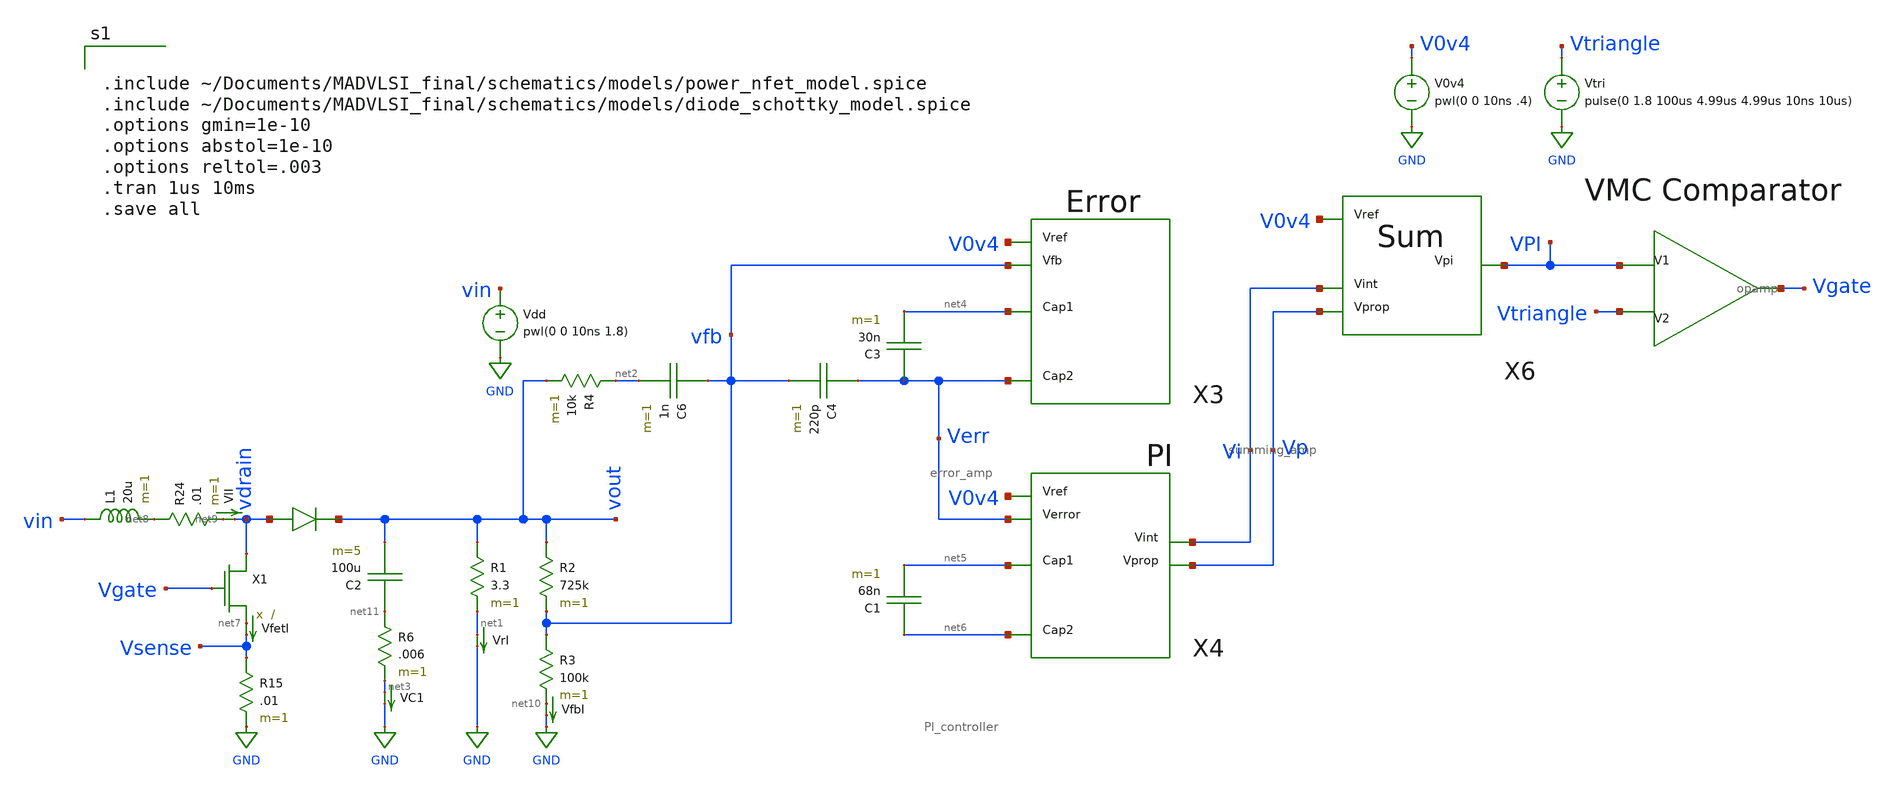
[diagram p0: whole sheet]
** sch_path: schematics/boost_controller_VMC.sch
**.subckt boost_controller_VMC
VfetI net7 Vsense 0
.save i(vfeti)
X1 vdrain Vgate net7 power_nfet
L1 vin net8 20u m=1
D1 vdrain vout diode_schottky
R1 vout net1 3.3 m=1
VlI net9 vdrain 0
.save i(vli)
VrI net1 GND 0
.save i(vri)
R2 vout vfb 725k m=1
R3 vfb net10 100k m=1
V0v4 V0v4 GND pwl(0 0 10ns .4)
R24 net8 net9 .01 m=1
VfbI net10 GND 0
.save i(vfbi)
C3 Verr net4 30n m=1
C4 Verr vfb 220p m=1
R4 net2 vout 10k m=1
C6 vfb net2 1n m=1
C2 net11 vout 100u m=5
R6 net11 net3 .006 m=1
VC1 net3 GND 0
.save i(vc1)
R15 Vsense GND .01 m=1
X3 V0v4 net4 vfb Verr error_amp
X4 V0v4 net5 Verr net6 Vi Vp PI_controller
C1 net6 net5 68n m=1
X6 V0v4 VPI Vi Vp summing_amp
X15 VPI Vtriangle Vgate opamp
Vtri Vtriangle GND pulse(0 1.8 100us 4.99us 4.99us 10ns 10us)
Vdd vin GND pwl(0 0 10ns 1.8)
**** begin user architecture code


.include ~/Documents/MADVLSI_final/schematics/models/power_nfet_model.spice
.include ~/Documents/MADVLSI_final/schematics/models/diode_schottky_model.spice
.options gmin=1e-10
.options abstol=1e-10
.options reltol=.003
.tran 1us 10ms
.save all


.option wnflag=1
.lib ~/skywater/skywater-pdk/libraries/sky130_fd_pr_ngspice/latest/models/sky130.lib.spice tt

**** end user architecture code
**.ends

* expanding   symbol:  /home/madvlsi/Documents/MADVLSI_final/schematics/error_amp.sym # of pins=4
** sym_path: schematics/error_amp.sym
** sch_path: schematics/error_amp.sch
.subckt error_amp Vref Cap1 Vfb Cap2
*.ipin Vfb
*.ipin Vref
*.iopin Cap1
*.iopin Cap2
XR1 Cap1 Vfb GND sky130_fd_pr__res_xhigh_po_0p35 L=8.65 mult=1 m=1
X1 Vref Vfb Cap2 opamp
.ends


* expanding   symbol:  /home/madvlsi/Documents/MADVLSI_final/schematics/PI_controller.sym # of
*+ pins=6
** sym_path: schematics/PI_controller.sym
** sch_path: schematics/PI_controller.sch
.subckt PI_controller Vref Cap1 Verror Cap2 Vint Vprop
*.ipin Verror
*.ipin Vref
*.iopin Cap1
*.iopin Cap2
*.opin Vint
*.opin Vprop
XR1 net1 net2 GND sky130_fd_pr__res_xhigh_po_0p35 L=1.65 mult=1 m=1
XR2 Vref net1 GND sky130_fd_pr__res_xhigh_po_0p35 L=1.65 mult=1 m=1
XR3 Verror Cap1 GND sky130_fd_pr__res_xhigh_po_0p35 L=1.65 mult=1 m=1
XR4 Cap1 Cap2 GND sky130_fd_pr__res_xhigh_po_0p35 L=8.65 mult=1 m=1
XR5 Cap2 net3 GND sky130_fd_pr__res_xhigh_po_0p35 L=1.65 mult=1 m=1
XR6 net3 Vint GND sky130_fd_pr__res_xhigh_po_0p35 L=8.65 mult=1 m=1
X1 Vref Cap1 Cap2 opamp
X2 Vref net3 Vint opamp
X3 net1 Vprop Vprop opamp
X4 Verror net2 net2 opamp
.ends


* expanding   symbol:  /home/madvlsi/Documents/MADVLSI_final/schematics/summing_amp.sym # of pins=4
** sym_path: schematics/summing_amp.sym
** sch_path: schematics/summing_amp.sch
.subckt summing_amp Vref Vpi Vint Vprop
*.ipin Vref
*.ipin Vint
*.ipin Vprop
*.opin Vpi
XR3 net1 Vint GND sky130_fd_pr__res_xhigh_po_0p35 L=1.65 mult=1 m=1
XR5 Vprop net1 GND sky130_fd_pr__res_xhigh_po_0p35 L=1.65 mult=1 m=1
XR1 net2 Vpi GND sky130_fd_pr__res_xhigh_po_0p35 L=1.65 mult=1 m=1
XR2 Vref net2 GND sky130_fd_pr__res_xhigh_po_0p35 L=1.65 mult=1 m=1
X1 net1 net2 Vpi opamp
.ends


* expanding   symbol:  /home/madvlsi/Documents/MADVLSI_final/schematics/opamp.sym # of pins=3
** sym_path: schematics/opamp.sym
** sch_path: schematics/opamp.sch
.subckt opamp V1 V2 VOUT
*.ipin V1
*.ipin V2
*.opin VOUT
XM19 net12 net10 GND VDD sky130_fd_pr__pfet_01v8 L=.6 W=1.5 nf=1 ad='int((nf+1)/2) * W/nf * 0.29' as='int((nf+2)/2) * W/nf * 0.29'
+ pd='2*int((nf+1)/2) * (W/nf + 0.29)' ps='2*int((nf+2)/2) * (W/nf + 0.29)' nrd='0.29 / W' nrs='0.29 / W'
+ sa=0 sb=0 sd=0 mult=1 m=1
XMD20 VDD VDD net12 VDD sky130_fd_pr__pfet_01v8 L=.6 W=1.5 nf=1 ad='int((nf+1)/2) * W/nf * 0.29' as='int((nf+2)/2) * W/nf * 0.29'
+ pd='2*int((nf+1)/2) * (W/nf + 0.29)' ps='2*int((nf+2)/2) * (W/nf + 0.29)' nrd='0.29 / W' nrs='0.29 / W'
+ sa=0 sb=0 sd=0 mult=1 m=1
XM22 net12 net10 net9 VDD sky130_fd_pr__pfet_01v8 L=.6 W=1.5 nf=1 ad='int((nf+1)/2) * W/nf * 0.29' as='int((nf+2)/2) * W/nf * 0.29'
+ pd='2*int((nf+1)/2) * (W/nf + 0.29)' ps='2*int((nf+2)/2) * (W/nf + 0.29)' nrd='0.29 / W' nrs='0.29 / W'
+ sa=0 sb=0 sd=0 mult=1 m=1
XM23 GND net10 net12 VDD sky130_fd_pr__pfet_01v8 L=.6 W=1.5 nf=1 ad='int((nf+1)/2) * W/nf * 0.29' as='int((nf+2)/2) * W/nf * 0.29'
+ pd='2*int((nf+1)/2) * (W/nf + 0.29)' ps='2*int((nf+2)/2) * (W/nf + 0.29)' nrd='0.29 / W' nrs='0.29 / W'
+ sa=0 sb=0 sd=0 mult=1 m=1
XMD24 net9 VDD net10 VDD sky130_fd_pr__pfet_01v8 L=.6 W=1.5 nf=1 ad='int((nf+1)/2) * W/nf * 0.29' as='int((nf+2)/2) * W/nf * 0.29'
+ pd='2*int((nf+1)/2) * (W/nf + 0.29)' ps='2*int((nf+2)/2) * (W/nf + 0.29)' nrd='0.29 / W' nrs='0.29 / W'
+ sa=0 sb=0 sd=0 mult=1 m=1
XM25 VDD net10 net12 VDD sky130_fd_pr__pfet_01v8 L=.6 W=1.5 nf=1 ad='int((nf+1)/2) * W/nf * 0.29' as='int((nf+2)/2) * W/nf * 0.29'
+ pd='2*int((nf+1)/2) * (W/nf + 0.29)' ps='2*int((nf+2)/2) * (W/nf + 0.29)' nrd='0.29 / W' nrs='0.29 / W'
+ sa=0 sb=0 sd=0 mult=1 m=1
XM26 net7 V2 net11 VDD sky130_fd_pr__pfet_01v8 L=.6 W=1.5 nf=1 ad='int((nf+1)/2) * W/nf * 0.29' as='int((nf+2)/2) * W/nf * 0.29'
+ pd='2*int((nf+1)/2) * (W/nf + 0.29)' ps='2*int((nf+2)/2) * (W/nf + 0.29)' nrd='0.29 / W' nrs='0.29 / W'
+ sa=0 sb=0 sd=0 mult=1 m=1
XMD27 net5 VDD net14 VDD sky130_fd_pr__pfet_01v8 L=.6 W=1.5 nf=1 ad='int((nf+1)/2) * W/nf * 0.29' as='int((nf+2)/2) * W/nf * 0.29'
+ pd='2*int((nf+1)/2) * (W/nf + 0.29)' ps='2*int((nf+2)/2) * (W/nf + 0.29)' nrd='0.29 / W' nrs='0.29 / W'
+ sa=0 sb=0 sd=0 mult=1 m=1
XM28 net6 V1 net11 VDD sky130_fd_pr__pfet_01v8 L=.6 W=1.5 nf=1 ad='int((nf+1)/2) * W/nf * 0.29' as='int((nf+2)/2) * W/nf * 0.29'
+ pd='2*int((nf+1)/2) * (W/nf + 0.29)' ps='2*int((nf+2)/2) * (W/nf + 0.29)' nrd='0.29 / W' nrs='0.29 / W'
+ sa=0 sb=0 sd=0 mult=1 m=1
XM29 net11 net10 VDD VDD sky130_fd_pr__pfet_01v8 L=.6 W=1.5 nf=1 ad='int((nf+1)/2) * W/nf * 0.29' as='int((nf+2)/2) * W/nf * 0.29'
+ pd='2*int((nf+1)/2) * (W/nf + 0.29)' ps='2*int((nf+2)/2) * (W/nf + 0.29)' nrd='0.29 / W' nrs='0.29 / W'
+ sa=0 sb=0 sd=0 mult=1 m=1
XMD30 net11 VDD VDD VDD sky130_fd_pr__pfet_01v8 L=.6 W=1.5 nf=1 ad='int((nf+1)/2) * W/nf * 0.29' as='int((nf+2)/2) * W/nf * 0.29'
+ pd='2*int((nf+1)/2) * (W/nf + 0.29)' ps='2*int((nf+2)/2) * (W/nf + 0.29)' nrd='0.29 / W' nrs='0.29 / W'
+ sa=0 sb=0 sd=0 mult=1 m=1
XMD31 net2 VDD net13 VDD sky130_fd_pr__pfet_01v8 L=.6 W=1.5 nf=1 ad='int((nf+1)/2) * W/nf * 0.29' as='int((nf+2)/2) * W/nf * 0.29'
+ pd='2*int((nf+1)/2) * (W/nf + 0.29)' ps='2*int((nf+2)/2) * (W/nf + 0.29)' nrd='0.29 / W' nrs='0.29 / W'
+ sa=0 sb=0 sd=0 mult=1 m=1
XM32 net4 net5 net5 VDD sky130_fd_pr__pfet_01v8 L=.6 W=1.5 nf=1 ad='int((nf+1)/2) * W/nf * 0.29' as='int((nf+2)/2) * W/nf * 0.29'
+ pd='2*int((nf+1)/2) * (W/nf + 0.29)' ps='2*int((nf+2)/2) * (W/nf + 0.29)' nrd='0.29 / W' nrs='0.29 / W'
+ sa=0 sb=0 sd=0 mult=1 m=1
XM33 VDD net10 net4 VDD sky130_fd_pr__pfet_01v8 L=.6 W=1.5 nf=1 ad='int((nf+1)/2) * W/nf * 0.29' as='int((nf+2)/2) * W/nf * 0.29'
+ pd='2*int((nf+1)/2) * (W/nf + 0.29)' ps='2*int((nf+2)/2) * (W/nf + 0.29)' nrd='0.29 / W' nrs='0.29 / W'
+ sa=0 sb=0 sd=0 mult=1 m=1
XM34 net3 net5 net2 VDD sky130_fd_pr__pfet_01v8 L=.6 W=1.5 nf=1 ad='int((nf+1)/2) * W/nf * 0.29' as='int((nf+2)/2) * W/nf * 0.29'
+ pd='2*int((nf+1)/2) * (W/nf + 0.29)' ps='2*int((nf+2)/2) * (W/nf + 0.29)' nrd='0.29 / W' nrs='0.29 / W'
+ sa=0 sb=0 sd=0 mult=1 m=1
XM35 VDD net10 net3 VDD sky130_fd_pr__pfet_01v8 L=.6 W=1.5 nf=1 ad='int((nf+1)/2) * W/nf * 0.29' as='int((nf+2)/2) * W/nf * 0.29'
+ pd='2*int((nf+1)/2) * (W/nf + 0.29)' ps='2*int((nf+2)/2) * (W/nf + 0.29)' nrd='0.29 / W' nrs='0.29 / W'
+ sa=0 sb=0 sd=0 mult=1 m=1
XM36 VOUT net2 VDD VDD sky130_fd_pr__pfet_01v8 L=.6 W=1.5 nf=1 ad='int((nf+1)/2) * W/nf * 0.29' as='int((nf+2)/2) * W/nf * 0.29'
+ pd='2*int((nf+1)/2) * (W/nf + 0.29)' ps='2*int((nf+2)/2) * (W/nf + 0.29)' nrd='0.29 / W' nrs='0.29 / W'
+ sa=0 sb=0 sd=0 mult=1 m=1
XM37 VDD net2 VOUT VDD sky130_fd_pr__pfet_01v8 L=.6 W=1.5 nf=1 ad='int((nf+1)/2) * W/nf * 0.29' as='int((nf+2)/2) * W/nf * 0.29'
+ pd='2*int((nf+1)/2) * (W/nf + 0.29)' ps='2*int((nf+2)/2) * (W/nf + 0.29)' nrd='0.29 / W' nrs='0.29 / W'
+ sa=0 sb=0 sd=0 mult=1 m=1
XM38 VOUT net2 VDD VDD sky130_fd_pr__pfet_01v8 L=.6 W=1.5 nf=1 ad='int((nf+1)/2) * W/nf * 0.29' as='int((nf+2)/2) * W/nf * 0.29'
+ pd='2*int((nf+1)/2) * (W/nf + 0.29)' ps='2*int((nf+2)/2) * (W/nf + 0.29)' nrd='0.29 / W' nrs='0.29 / W'
+ sa=0 sb=0 sd=0 mult=1 m=1
XM39 VDD net2 VOUT VDD sky130_fd_pr__pfet_01v8 L=.6 W=1.5 nf=1 ad='int((nf+1)/2) * W/nf * 0.29' as='int((nf+2)/2) * W/nf * 0.29'
+ pd='2*int((nf+1)/2) * (W/nf + 0.29)' ps='2*int((nf+2)/2) * (W/nf + 0.29)' nrd='0.29 / W' nrs='0.29 / W'
+ sa=0 sb=0 sd=0 mult=1 m=1
XM40 net1 net9 VDD GND sky130_fd_pr__nfet_01v8 L=.6 W=1.5 nf=1 ad='int((nf+1)/2) * W/nf * 0.29' as='int((nf+2)/2) * W/nf * 0.29'
+ pd='2*int((nf+1)/2) * (W/nf + 0.29)' ps='2*int((nf+2)/2) * (W/nf + 0.29)' nrd='0.29 / W' nrs='0.29 / W'
+ sa=0 sb=0 sd=0 mult=1 m=1
XMD41 GND GND net1 GND sky130_fd_pr__nfet_01v8 L=.6 W=1.5 nf=1 ad='int((nf+1)/2) * W/nf * 0.29' as='int((nf+2)/2) * W/nf * 0.29'
+ pd='2*int((nf+1)/2) * (W/nf + 0.29)' ps='2*int((nf+2)/2) * (W/nf + 0.29)' nrd='0.29 / W' nrs='0.29 / W'
+ sa=0 sb=0 sd=0 mult=1 m=1
XM42 net1 net9 net10 GND sky130_fd_pr__nfet_01v8 L=.6 W=1.5 nf=1 ad='int((nf+1)/2) * W/nf * 0.29' as='int((nf+2)/2) * W/nf * 0.29'
+ pd='2*int((nf+1)/2) * (W/nf + 0.29)' ps='2*int((nf+2)/2) * (W/nf + 0.29)' nrd='0.29 / W' nrs='0.29 / W'
+ sa=0 sb=0 sd=0 mult=1 m=1
XM43 VDD net9 net1 GND sky130_fd_pr__nfet_01v8 L=.6 W=1.5 nf=1 ad='int((nf+1)/2) * W/nf * 0.29' as='int((nf+2)/2) * W/nf * 0.29'
+ pd='2*int((nf+1)/2) * (W/nf + 0.29)' ps='2*int((nf+2)/2) * (W/nf + 0.29)' nrd='0.29 / W' nrs='0.29 / W'
+ sa=0 sb=0 sd=0 mult=1 m=1
XMD44 net10 GND net9 GND sky130_fd_pr__nfet_01v8 L=.6 W=1.5 nf=1 ad='int((nf+1)/2) * W/nf * 0.29' as='int((nf+2)/2) * W/nf * 0.29'
+ pd='2*int((nf+1)/2) * (W/nf + 0.29)' ps='2*int((nf+2)/2) * (W/nf + 0.29)' nrd='0.29 / W' nrs='0.29 / W'
+ sa=0 sb=0 sd=0 mult=1 m=1
XM45 GND net9 net1 GND sky130_fd_pr__nfet_01v8 L=.6 W=1.5 nf=1 ad='int((nf+1)/2) * W/nf * 0.29' as='int((nf+2)/2) * W/nf * 0.29'
+ pd='2*int((nf+1)/2) * (W/nf + 0.29)' ps='2*int((nf+2)/2) * (W/nf + 0.29)' nrd='0.29 / W' nrs='0.29 / W'
+ sa=0 sb=0 sd=0 mult=1 m=1
XM46 net3 V1 net8 GND sky130_fd_pr__nfet_01v8 L=.6 W=1.5 nf=1 ad='int((nf+1)/2) * W/nf * 0.29' as='int((nf+2)/2) * W/nf * 0.29'
+ pd='2*int((nf+1)/2) * (W/nf + 0.29)' ps='2*int((nf+2)/2) * (W/nf + 0.29)' nrd='0.29 / W' nrs='0.29 / W'
+ sa=0 sb=0 sd=0 mult=1 m=1
XMD47 net5 GND net15 GND sky130_fd_pr__nfet_01v8 L=.6 W=1.5 nf=1 ad='int((nf+1)/2) * W/nf * 0.29' as='int((nf+2)/2) * W/nf * 0.29'
+ pd='2*int((nf+1)/2) * (W/nf + 0.29)' ps='2*int((nf+2)/2) * (W/nf + 0.29)' nrd='0.29 / W' nrs='0.29 / W'
+ sa=0 sb=0 sd=0 mult=1 m=1
XM48 net4 V2 net8 GND sky130_fd_pr__nfet_01v8 L=.6 W=1.5 nf=1 ad='int((nf+1)/2) * W/nf * 0.29' as='int((nf+2)/2) * W/nf * 0.29'
+ pd='2*int((nf+1)/2) * (W/nf + 0.29)' ps='2*int((nf+2)/2) * (W/nf + 0.29)' nrd='0.29 / W' nrs='0.29 / W'
+ sa=0 sb=0 sd=0 mult=1 m=1
XM49 net8 net9 GND GND sky130_fd_pr__nfet_01v8 L=.6 W=1.5 nf=1 ad='int((nf+1)/2) * W/nf * 0.29' as='int((nf+2)/2) * W/nf * 0.29'
+ pd='2*int((nf+1)/2) * (W/nf + 0.29)' ps='2*int((nf+2)/2) * (W/nf + 0.29)' nrd='0.29 / W' nrs='0.29 / W'
+ sa=0 sb=0 sd=0 mult=1 m=1
XMD50 net8 GND GND GND sky130_fd_pr__nfet_01v8 L=.6 W=1.5 nf=1 ad='int((nf+1)/2) * W/nf * 0.29' as='int((nf+2)/2) * W/nf * 0.29'
+ pd='2*int((nf+1)/2) * (W/nf + 0.29)' ps='2*int((nf+2)/2) * (W/nf + 0.29)' nrd='0.29 / W' nrs='0.29 / W'
+ sa=0 sb=0 sd=0 mult=1 m=1
XMD51 net2 GND net16 GND sky130_fd_pr__nfet_01v8 L=.6 W=1.5 nf=1 ad='int((nf+1)/2) * W/nf * 0.29' as='int((nf+2)/2) * W/nf * 0.29'
+ pd='2*int((nf+1)/2) * (W/nf + 0.29)' ps='2*int((nf+2)/2) * (W/nf + 0.29)' nrd='0.29 / W' nrs='0.29 / W'
+ sa=0 sb=0 sd=0 mult=1 m=1
XM52 GND net9 net7 GND sky130_fd_pr__nfet_01v8 L=.6 W=1.5 nf=1 ad='int((nf+1)/2) * W/nf * 0.29' as='int((nf+2)/2) * W/nf * 0.29'
+ pd='2*int((nf+1)/2) * (W/nf + 0.29)' ps='2*int((nf+2)/2) * (W/nf + 0.29)' nrd='0.29 / W' nrs='0.29 / W'
+ sa=0 sb=0 sd=0 mult=1 m=1
XMD53 VOUT GND GND GND sky130_fd_pr__nfet_01v8 L=.6 W=1.5 nf=1 ad='int((nf+1)/2) * W/nf * 0.29' as='int((nf+2)/2) * W/nf * 0.29'
+ pd='2*int((nf+1)/2) * (W/nf + 0.29)' ps='2*int((nf+2)/2) * (W/nf + 0.29)' nrd='0.29 / W' nrs='0.29 / W'
+ sa=0 sb=0 sd=0 mult=1 m=1
XM54 GND net9 net6 GND sky130_fd_pr__nfet_01v8 L=.6 W=1.5 nf=1 ad='int((nf+1)/2) * W/nf * 0.29' as='int((nf+2)/2) * W/nf * 0.29'
+ pd='2*int((nf+1)/2) * (W/nf + 0.29)' ps='2*int((nf+2)/2) * (W/nf + 0.29)' nrd='0.29 / W' nrs='0.29 / W'
+ sa=0 sb=0 sd=0 mult=1 m=1
XM55 net7 net5 net5 GND sky130_fd_pr__nfet_01v8 L=.6 W=1.5 nf=1 ad='int((nf+1)/2) * W/nf * 0.29' as='int((nf+2)/2) * W/nf * 0.29'
+ pd='2*int((nf+1)/2) * (W/nf + 0.29)' ps='2*int((nf+2)/2) * (W/nf + 0.29)' nrd='0.29 / W' nrs='0.29 / W'
+ sa=0 sb=0 sd=0 mult=1 m=1
XM56 net6 net5 net2 GND sky130_fd_pr__nfet_01v8 L=.6 W=1.5 nf=1 ad='int((nf+1)/2) * W/nf * 0.29' as='int((nf+2)/2) * W/nf * 0.29'
+ pd='2*int((nf+1)/2) * (W/nf + 0.29)' ps='2*int((nf+2)/2) * (W/nf + 0.29)' nrd='0.29 / W' nrs='0.29 / W'
+ sa=0 sb=0 sd=0 mult=1 m=1
XMD57 VOUT GND GND GND sky130_fd_pr__nfet_01v8 L=.6 W=1.5 nf=1 ad='int((nf+1)/2) * W/nf * 0.29' as='int((nf+2)/2) * W/nf * 0.29'
+ pd='2*int((nf+1)/2) * (W/nf + 0.29)' ps='2*int((nf+2)/2) * (W/nf + 0.29)' nrd='0.29 / W' nrs='0.29 / W'
+ sa=0 sb=0 sd=0 mult=1 m=1
XM58 GND net2 VOUT GND sky130_fd_pr__nfet_01v8 L=.6 W=1.5 nf=1 ad='int((nf+1)/2) * W/nf * 0.29' as='int((nf+2)/2) * W/nf * 0.29'
+ pd='2*int((nf+1)/2) * (W/nf + 0.29)' ps='2*int((nf+2)/2) * (W/nf + 0.29)' nrd='0.29 / W' nrs='0.29 / W'
+ sa=0 sb=0 sd=0 mult=1 m=1
XM59 GND net2 VOUT GND sky130_fd_pr__nfet_01v8 L=.6 W=1.5 nf=1 ad='int((nf+1)/2) * W/nf * 0.29' as='int((nf+2)/2) * W/nf * 0.29'
+ pd='2*int((nf+1)/2) * (W/nf + 0.29)' ps='2*int((nf+2)/2) * (W/nf + 0.29)' nrd='0.29 / W' nrs='0.29 / W'
+ sa=0 sb=0 sd=0 mult=1 m=1
XM60 net12 net10 GND VDD sky130_fd_pr__pfet_01v8 L=.6 W=1.5 nf=1 ad='int((nf+1)/2) * W/nf * 0.29' as='int((nf+2)/2) * W/nf * 0.29'
+ pd='2*int((nf+1)/2) * (W/nf + 0.29)' ps='2*int((nf+2)/2) * (W/nf + 0.29)' nrd='0.29 / W' nrs='0.29 / W'
+ sa=0 sb=0 sd=0 mult=1 m=1
XM61 net10 net10 net4 VDD sky130_fd_pr__pfet_01v8 L=.6 W=1.5 nf=1 ad='int((nf+1)/2) * W/nf * 0.29' as='int((nf+2)/2) * W/nf * 0.29'
+ pd='2*int((nf+1)/2) * (W/nf + 0.29)' ps='2*int((nf+2)/2) * (W/nf + 0.29)' nrd='0.29 / W' nrs='0.29 / W'
+ sa=0 sb=0 sd=0 mult=1 m=1
XM62 net1 net9 VDD GND sky130_fd_pr__nfet_01v8 L=.6 W=1.5 nf=1 ad='int((nf+1)/2) * W/nf * 0.29' as='int((nf+2)/2) * W/nf * 0.29'
+ pd='2*int((nf+1)/2) * (W/nf + 0.29)' ps='2*int((nf+2)/2) * (W/nf + 0.29)' nrd='0.29 / W' nrs='0.29 / W'
+ sa=0 sb=0 sd=0 mult=1 m=1
XM63 net9 net9 net7 GND sky130_fd_pr__nfet_01v8 L=.6 W=1.5 nf=1 ad='int((nf+1)/2) * W/nf * 0.29' as='int((nf+2)/2) * W/nf * 0.29'
+ pd='2*int((nf+1)/2) * (W/nf + 0.29)' ps='2*int((nf+2)/2) * (W/nf + 0.29)' nrd='0.29 / W' nrs='0.29 / W'
+ sa=0 sb=0 sd=0 mult=1 m=1
XMD64 VDD GND GND GND sky130_fd_pr__nfet_01v8 L=.6 W=1.5 nf=1 ad='int((nf+1)/2) * W/nf * 0.29' as='int((nf+2)/2) * W/nf * 0.29'
+ pd='2*int((nf+1)/2) * (W/nf + 0.29)' ps='2*int((nf+2)/2) * (W/nf + 0.29)' nrd='0.29 / W' nrs='0.29 / W'
+ sa=0 sb=0 sd=0 mult=1 m=1
XMD65 net7 GND GND GND sky130_fd_pr__nfet_01v8 L=.6 W=1.5 nf=1 ad='int((nf+1)/2) * W/nf * 0.29' as='int((nf+2)/2) * W/nf * 0.29'
+ pd='2*int((nf+1)/2) * (W/nf + 0.29)' ps='2*int((nf+2)/2) * (W/nf + 0.29)' nrd='0.29 / W' nrs='0.29 / W'
+ sa=0 sb=0 sd=0 mult=1 m=1
XMD66 GND VDD VDD VDD sky130_fd_pr__pfet_01v8 L=.6 W=1.5 nf=1 ad='int((nf+1)/2) * W/nf * 0.29' as='int((nf+2)/2) * W/nf * 0.29'
+ pd='2*int((nf+1)/2) * (W/nf + 0.29)' ps='2*int((nf+2)/2) * (W/nf + 0.29)' nrd='0.29 / W' nrs='0.29 / W'
+ sa=0 sb=0 sd=0 mult=1 m=1
XMD67 net4 VDD VDD VDD sky130_fd_pr__pfet_01v8 L=.6 W=1.5 nf=1 ad='int((nf+1)/2) * W/nf * 0.29' as='int((nf+2)/2) * W/nf * 0.29'
+ pd='2*int((nf+1)/2) * (W/nf + 0.29)' ps='2*int((nf+2)/2) * (W/nf + 0.29)' nrd='0.29 / W' nrs='0.29 / W'
+ sa=0 sb=0 sd=0 mult=1 m=1
XMD1 net15 GND net3 GND sky130_fd_pr__nfet_01v8 L=.6 W=1.5 nf=1 ad='int((nf+1)/2) * W/nf * 0.29' as='int((nf+2)/2) * W/nf * 0.29'
+ pd='2*int((nf+1)/2) * (W/nf + 0.29)' ps='2*int((nf+2)/2) * (W/nf + 0.29)' nrd='0.29 / W' nrs='0.29 / W'
+ sa=0 sb=0 sd=0 mult=1 m=1
XMD2 net16 GND net4 GND sky130_fd_pr__nfet_01v8 L=.6 W=1.5 nf=1 ad='int((nf+1)/2) * W/nf * 0.29' as='int((nf+2)/2) * W/nf * 0.29'
+ pd='2*int((nf+1)/2) * (W/nf + 0.29)' ps='2*int((nf+2)/2) * (W/nf + 0.29)' nrd='0.29 / W' nrs='0.29 / W'
+ sa=0 sb=0 sd=0 mult=1 m=1
XMD3 net13 VDD net6 VDD sky130_fd_pr__pfet_01v8 L=.6 W=1.5 nf=1 ad='int((nf+1)/2) * W/nf * 0.29' as='int((nf+2)/2) * W/nf * 0.29'
+ pd='2*int((nf+1)/2) * (W/nf + 0.29)' ps='2*int((nf+2)/2) * (W/nf + 0.29)' nrd='0.29 / W' nrs='0.29 / W'
+ sa=0 sb=0 sd=0 mult=1 m=1
XMD4 net14 VDD net7 VDD sky130_fd_pr__pfet_01v8 L=.6 W=1.5 nf=1 ad='int((nf+1)/2) * W/nf * 0.29' as='int((nf+2)/2) * W/nf * 0.29'
+ pd='2*int((nf+1)/2) * (W/nf + 0.29)' ps='2*int((nf+2)/2) * (W/nf + 0.29)' nrd='0.29 / W' nrs='0.29 / W'
+ sa=0 sb=0 sd=0 mult=1 m=1
XM1 net21 net10 GND VDD sky130_fd_pr__pfet_01v8 L=.6 W=1.5 nf=1 ad='int((nf+1)/2) * W/nf * 0.29' as='int((nf+2)/2) * W/nf * 0.29'
+ pd='2*int((nf+1)/2) * (W/nf + 0.29)' ps='2*int((nf+2)/2) * (W/nf + 0.29)' nrd='0.29 / W' nrs='0.29 / W'
+ sa=0 sb=0 sd=0 mult=1 m=1
XMD5 VDD VDD net21 VDD sky130_fd_pr__pfet_01v8 L=.6 W=1.5 nf=1 ad='int((nf+1)/2) * W/nf * 0.29' as='int((nf+2)/2) * W/nf * 0.29'
+ pd='2*int((nf+1)/2) * (W/nf + 0.29)' ps='2*int((nf+2)/2) * (W/nf + 0.29)' nrd='0.29 / W' nrs='0.29 / W'
+ sa=0 sb=0 sd=0 mult=1 m=1
XM6 net21 net10 net9 VDD sky130_fd_pr__pfet_01v8 L=.6 W=1.5 nf=1 ad='int((nf+1)/2) * W/nf * 0.29' as='int((nf+2)/2) * W/nf * 0.29'
+ pd='2*int((nf+1)/2) * (W/nf + 0.29)' ps='2*int((nf+2)/2) * (W/nf + 0.29)' nrd='0.29 / W' nrs='0.29 / W'
+ sa=0 sb=0 sd=0 mult=1 m=1
XM7 GND net10 net21 VDD sky130_fd_pr__pfet_01v8 L=.6 W=1.5 nf=1 ad='int((nf+1)/2) * W/nf * 0.29' as='int((nf+2)/2) * W/nf * 0.29'
+ pd='2*int((nf+1)/2) * (W/nf + 0.29)' ps='2*int((nf+2)/2) * (W/nf + 0.29)' nrd='0.29 / W' nrs='0.29 / W'
+ sa=0 sb=0 sd=0 mult=1 m=1
XMD8 net9 VDD net10 VDD sky130_fd_pr__pfet_01v8 L=.6 W=1.5 nf=1 ad='int((nf+1)/2) * W/nf * 0.29' as='int((nf+2)/2) * W/nf * 0.29'
+ pd='2*int((nf+1)/2) * (W/nf + 0.29)' ps='2*int((nf+2)/2) * (W/nf + 0.29)' nrd='0.29 / W' nrs='0.29 / W'
+ sa=0 sb=0 sd=0 mult=1 m=1
XM9 VDD net10 net21 VDD sky130_fd_pr__pfet_01v8 L=.6 W=1.5 nf=1 ad='int((nf+1)/2) * W/nf * 0.29' as='int((nf+2)/2) * W/nf * 0.29'
+ pd='2*int((nf+1)/2) * (W/nf + 0.29)' ps='2*int((nf+2)/2) * (W/nf + 0.29)' nrd='0.29 / W' nrs='0.29 / W'
+ sa=0 sb=0 sd=0 mult=1 m=1
XM10 net7 V2 net20 VDD sky130_fd_pr__pfet_01v8 L=.6 W=1.5 nf=1 ad='int((nf+1)/2) * W/nf * 0.29' as='int((nf+2)/2) * W/nf * 0.29'
+ pd='2*int((nf+1)/2) * (W/nf + 0.29)' ps='2*int((nf+2)/2) * (W/nf + 0.29)' nrd='0.29 / W' nrs='0.29 / W'
+ sa=0 sb=0 sd=0 mult=1 m=1
XMD11 net18 VDD net23 VDD sky130_fd_pr__pfet_01v8 L=.6 W=1.5 nf=1 ad='int((nf+1)/2) * W/nf * 0.29' as='int((nf+2)/2) * W/nf * 0.29'
+ pd='2*int((nf+1)/2) * (W/nf + 0.29)' ps='2*int((nf+2)/2) * (W/nf + 0.29)' nrd='0.29 / W' nrs='0.29 / W'
+ sa=0 sb=0 sd=0 mult=1 m=1
XM12 net6 V1 net20 VDD sky130_fd_pr__pfet_01v8 L=.6 W=1.5 nf=1 ad='int((nf+1)/2) * W/nf * 0.29' as='int((nf+2)/2) * W/nf * 0.29'
+ pd='2*int((nf+1)/2) * (W/nf + 0.29)' ps='2*int((nf+2)/2) * (W/nf + 0.29)' nrd='0.29 / W' nrs='0.29 / W'
+ sa=0 sb=0 sd=0 mult=1 m=1
XM13 net20 net10 VDD VDD sky130_fd_pr__pfet_01v8 L=.6 W=1.5 nf=1 ad='int((nf+1)/2) * W/nf * 0.29' as='int((nf+2)/2) * W/nf * 0.29'
+ pd='2*int((nf+1)/2) * (W/nf + 0.29)' ps='2*int((nf+2)/2) * (W/nf + 0.29)' nrd='0.29 / W' nrs='0.29 / W'
+ sa=0 sb=0 sd=0 mult=1 m=1
XMD14 net20 VDD VDD VDD sky130_fd_pr__pfet_01v8 L=.6 W=1.5 nf=1 ad='int((nf+1)/2) * W/nf * 0.29' as='int((nf+2)/2) * W/nf * 0.29'
+ pd='2*int((nf+1)/2) * (W/nf + 0.29)' ps='2*int((nf+2)/2) * (W/nf + 0.29)' nrd='0.29 / W' nrs='0.29 / W'
+ sa=0 sb=0 sd=0 mult=1 m=1
XMD15 net2 VDD net22 VDD sky130_fd_pr__pfet_01v8 L=.6 W=1.5 nf=1 ad='int((nf+1)/2) * W/nf * 0.29' as='int((nf+2)/2) * W/nf * 0.29'
+ pd='2*int((nf+1)/2) * (W/nf + 0.29)' ps='2*int((nf+2)/2) * (W/nf + 0.29)' nrd='0.29 / W' nrs='0.29 / W'
+ sa=0 sb=0 sd=0 mult=1 m=1
XM16 net4 net18 net18 VDD sky130_fd_pr__pfet_01v8 L=.6 W=1.5 nf=1 ad='int((nf+1)/2) * W/nf * 0.29' as='int((nf+2)/2) * W/nf * 0.29'
+ pd='2*int((nf+1)/2) * (W/nf + 0.29)' ps='2*int((nf+2)/2) * (W/nf + 0.29)' nrd='0.29 / W' nrs='0.29 / W'
+ sa=0 sb=0 sd=0 mult=1 m=1
XM17 VDD net10 net4 VDD sky130_fd_pr__pfet_01v8 L=.6 W=1.5 nf=1 ad='int((nf+1)/2) * W/nf * 0.29' as='int((nf+2)/2) * W/nf * 0.29'
+ pd='2*int((nf+1)/2) * (W/nf + 0.29)' ps='2*int((nf+2)/2) * (W/nf + 0.29)' nrd='0.29 / W' nrs='0.29 / W'
+ sa=0 sb=0 sd=0 mult=1 m=1
XM18 net3 net18 net2 VDD sky130_fd_pr__pfet_01v8 L=.6 W=1.5 nf=1 ad='int((nf+1)/2) * W/nf * 0.29' as='int((nf+2)/2) * W/nf * 0.29'
+ pd='2*int((nf+1)/2) * (W/nf + 0.29)' ps='2*int((nf+2)/2) * (W/nf + 0.29)' nrd='0.29 / W' nrs='0.29 / W'
+ sa=0 sb=0 sd=0 mult=1 m=1
XM20 VDD net10 net3 VDD sky130_fd_pr__pfet_01v8 L=.6 W=1.5 nf=1 ad='int((nf+1)/2) * W/nf * 0.29' as='int((nf+2)/2) * W/nf * 0.29'
+ pd='2*int((nf+1)/2) * (W/nf + 0.29)' ps='2*int((nf+2)/2) * (W/nf + 0.29)' nrd='0.29 / W' nrs='0.29 / W'
+ sa=0 sb=0 sd=0 mult=1 m=1
XM21 VOUT net2 VDD VDD sky130_fd_pr__pfet_01v8 L=.6 W=1.5 nf=1 ad='int((nf+1)/2) * W/nf * 0.29' as='int((nf+2)/2) * W/nf * 0.29'
+ pd='2*int((nf+1)/2) * (W/nf + 0.29)' ps='2*int((nf+2)/2) * (W/nf + 0.29)' nrd='0.29 / W' nrs='0.29 / W'
+ sa=0 sb=0 sd=0 mult=1 m=1
XM24 VDD net2 VOUT VDD sky130_fd_pr__pfet_01v8 L=.6 W=1.5 nf=1 ad='int((nf+1)/2) * W/nf * 0.29' as='int((nf+2)/2) * W/nf * 0.29'
+ pd='2*int((nf+1)/2) * (W/nf + 0.29)' ps='2*int((nf+2)/2) * (W/nf + 0.29)' nrd='0.29 / W' nrs='0.29 / W'
+ sa=0 sb=0 sd=0 mult=1 m=1
XM27 VOUT net2 VDD VDD sky130_fd_pr__pfet_01v8 L=.6 W=1.5 nf=1 ad='int((nf+1)/2) * W/nf * 0.29' as='int((nf+2)/2) * W/nf * 0.29'
+ pd='2*int((nf+1)/2) * (W/nf + 0.29)' ps='2*int((nf+2)/2) * (W/nf + 0.29)' nrd='0.29 / W' nrs='0.29 / W'
+ sa=0 sb=0 sd=0 mult=1 m=1
XM30 VDD net2 VOUT VDD sky130_fd_pr__pfet_01v8 L=.6 W=1.5 nf=1 ad='int((nf+1)/2) * W/nf * 0.29' as='int((nf+2)/2) * W/nf * 0.29'
+ pd='2*int((nf+1)/2) * (W/nf + 0.29)' ps='2*int((nf+2)/2) * (W/nf + 0.29)' nrd='0.29 / W' nrs='0.29 / W'
+ sa=0 sb=0 sd=0 mult=1 m=1
XM31 net17 net9 VDD GND sky130_fd_pr__nfet_01v8 L=.6 W=1.5 nf=1 ad='int((nf+1)/2) * W/nf * 0.29' as='int((nf+2)/2) * W/nf * 0.29'
+ pd='2*int((nf+1)/2) * (W/nf + 0.29)' ps='2*int((nf+2)/2) * (W/nf + 0.29)' nrd='0.29 / W' nrs='0.29 / W'
+ sa=0 sb=0 sd=0 mult=1 m=1
XMD32 GND GND net17 GND sky130_fd_pr__nfet_01v8 L=.6 W=1.5 nf=1 ad='int((nf+1)/2) * W/nf * 0.29' as='int((nf+2)/2) * W/nf * 0.29'
+ pd='2*int((nf+1)/2) * (W/nf + 0.29)' ps='2*int((nf+2)/2) * (W/nf + 0.29)' nrd='0.29 / W' nrs='0.29 / W'
+ sa=0 sb=0 sd=0 mult=1 m=1
XM41 net17 net9 net10 GND sky130_fd_pr__nfet_01v8 L=.6 W=1.5 nf=1 ad='int((nf+1)/2) * W/nf * 0.29' as='int((nf+2)/2) * W/nf * 0.29'
+ pd='2*int((nf+1)/2) * (W/nf + 0.29)' ps='2*int((nf+2)/2) * (W/nf + 0.29)' nrd='0.29 / W' nrs='0.29 / W'
+ sa=0 sb=0 sd=0 mult=1 m=1
XM44 VDD net9 net17 GND sky130_fd_pr__nfet_01v8 L=.6 W=1.5 nf=1 ad='int((nf+1)/2) * W/nf * 0.29' as='int((nf+2)/2) * W/nf * 0.29'
+ pd='2*int((nf+1)/2) * (W/nf + 0.29)' ps='2*int((nf+2)/2) * (W/nf + 0.29)' nrd='0.29 / W' nrs='0.29 / W'
+ sa=0 sb=0 sd=0 mult=1 m=1
XMD45 net10 GND net9 GND sky130_fd_pr__nfet_01v8 L=.6 W=1.5 nf=1 ad='int((nf+1)/2) * W/nf * 0.29' as='int((nf+2)/2) * W/nf * 0.29'
+ pd='2*int((nf+1)/2) * (W/nf + 0.29)' ps='2*int((nf+2)/2) * (W/nf + 0.29)' nrd='0.29 / W' nrs='0.29 / W'
+ sa=0 sb=0 sd=0 mult=1 m=1
XM47 GND net9 net17 GND sky130_fd_pr__nfet_01v8 L=.6 W=1.5 nf=1 ad='int((nf+1)/2) * W/nf * 0.29' as='int((nf+2)/2) * W/nf * 0.29'
+ pd='2*int((nf+1)/2) * (W/nf + 0.29)' ps='2*int((nf+2)/2) * (W/nf + 0.29)' nrd='0.29 / W' nrs='0.29 / W'
+ sa=0 sb=0 sd=0 mult=1 m=1
XM50 net3 V1 net19 GND sky130_fd_pr__nfet_01v8 L=.6 W=1.5 nf=1 ad='int((nf+1)/2) * W/nf * 0.29' as='int((nf+2)/2) * W/nf * 0.29'
+ pd='2*int((nf+1)/2) * (W/nf + 0.29)' ps='2*int((nf+2)/2) * (W/nf + 0.29)' nrd='0.29 / W' nrs='0.29 / W'
+ sa=0 sb=0 sd=0 mult=1 m=1
XMD52 net18 GND net24 GND sky130_fd_pr__nfet_01v8 L=.6 W=1.5 nf=1 ad='int((nf+1)/2) * W/nf * 0.29' as='int((nf+2)/2) * W/nf * 0.29'
+ pd='2*int((nf+1)/2) * (W/nf + 0.29)' ps='2*int((nf+2)/2) * (W/nf + 0.29)' nrd='0.29 / W' nrs='0.29 / W'
+ sa=0 sb=0 sd=0 mult=1 m=1
XM53 net4 V2 net19 GND sky130_fd_pr__nfet_01v8 L=.6 W=1.5 nf=1 ad='int((nf+1)/2) * W/nf * 0.29' as='int((nf+2)/2) * W/nf * 0.29'
+ pd='2*int((nf+1)/2) * (W/nf + 0.29)' ps='2*int((nf+2)/2) * (W/nf + 0.29)' nrd='0.29 / W' nrs='0.29 / W'
+ sa=0 sb=0 sd=0 mult=1 m=1
XM57 net19 net9 GND GND sky130_fd_pr__nfet_01v8 L=.6 W=1.5 nf=1 ad='int((nf+1)/2) * W/nf * 0.29' as='int((nf+2)/2) * W/nf * 0.29'
+ pd='2*int((nf+1)/2) * (W/nf + 0.29)' ps='2*int((nf+2)/2) * (W/nf + 0.29)' nrd='0.29 / W' nrs='0.29 / W'
+ sa=0 sb=0 sd=0 mult=1 m=1
XMD58 net19 GND GND GND sky130_fd_pr__nfet_01v8 L=.6 W=1.5 nf=1 ad='int((nf+1)/2) * W/nf * 0.29' as='int((nf+2)/2) * W/nf * 0.29'
+ pd='2*int((nf+1)/2) * (W/nf + 0.29)' ps='2*int((nf+2)/2) * (W/nf + 0.29)' nrd='0.29 / W' nrs='0.29 / W'
+ sa=0 sb=0 sd=0 mult=1 m=1
XMD59 net2 GND net25 GND sky130_fd_pr__nfet_01v8 L=.6 W=1.5 nf=1 ad='int((nf+1)/2) * W/nf * 0.29' as='int((nf+2)/2) * W/nf * 0.29'
+ pd='2*int((nf+1)/2) * (W/nf + 0.29)' ps='2*int((nf+2)/2) * (W/nf + 0.29)' nrd='0.29 / W' nrs='0.29 / W'
+ sa=0 sb=0 sd=0 mult=1 m=1
XM64 GND net9 net7 GND sky130_fd_pr__nfet_01v8 L=.6 W=1.5 nf=1 ad='int((nf+1)/2) * W/nf * 0.29' as='int((nf+2)/2) * W/nf * 0.29'
+ pd='2*int((nf+1)/2) * (W/nf + 0.29)' ps='2*int((nf+2)/2) * (W/nf + 0.29)' nrd='0.29 / W' nrs='0.29 / W'
+ sa=0 sb=0 sd=0 mult=1 m=1
XMD68 VOUT GND GND GND sky130_fd_pr__nfet_01v8 L=.6 W=1.5 nf=1 ad='int((nf+1)/2) * W/nf * 0.29' as='int((nf+2)/2) * W/nf * 0.29'
+ pd='2*int((nf+1)/2) * (W/nf + 0.29)' ps='2*int((nf+2)/2) * (W/nf + 0.29)' nrd='0.29 / W' nrs='0.29 / W'
+ sa=0 sb=0 sd=0 mult=1 m=1
XM69 GND net9 net6 GND sky130_fd_pr__nfet_01v8 L=.6 W=1.5 nf=1 ad='int((nf+1)/2) * W/nf * 0.29' as='int((nf+2)/2) * W/nf * 0.29'
+ pd='2*int((nf+1)/2) * (W/nf + 0.29)' ps='2*int((nf+2)/2) * (W/nf + 0.29)' nrd='0.29 / W' nrs='0.29 / W'
+ sa=0 sb=0 sd=0 mult=1 m=1
XM70 net7 net18 net18 GND sky130_fd_pr__nfet_01v8 L=.6 W=1.5 nf=1 ad='int((nf+1)/2) * W/nf * 0.29' as='int((nf+2)/2) * W/nf * 0.29'
+ pd='2*int((nf+1)/2) * (W/nf + 0.29)' ps='2*int((nf+2)/2) * (W/nf + 0.29)' nrd='0.29 / W' nrs='0.29 / W'
+ sa=0 sb=0 sd=0 mult=1 m=1
XM71 net6 net18 net2 GND sky130_fd_pr__nfet_01v8 L=.6 W=1.5 nf=1 ad='int((nf+1)/2) * W/nf * 0.29' as='int((nf+2)/2) * W/nf * 0.29'
+ pd='2*int((nf+1)/2) * (W/nf + 0.29)' ps='2*int((nf+2)/2) * (W/nf + 0.29)' nrd='0.29 / W' nrs='0.29 / W'
+ sa=0 sb=0 sd=0 mult=1 m=1
XMD72 VOUT GND GND GND sky130_fd_pr__nfet_01v8 L=.6 W=1.5 nf=1 ad='int((nf+1)/2) * W/nf * 0.29' as='int((nf+2)/2) * W/nf * 0.29'
+ pd='2*int((nf+1)/2) * (W/nf + 0.29)' ps='2*int((nf+2)/2) * (W/nf + 0.29)' nrd='0.29 / W' nrs='0.29 / W'
+ sa=0 sb=0 sd=0 mult=1 m=1
XM73 GND net2 VOUT GND sky130_fd_pr__nfet_01v8 L=.6 W=1.5 nf=1 ad='int((nf+1)/2) * W/nf * 0.29' as='int((nf+2)/2) * W/nf * 0.29'
+ pd='2*int((nf+1)/2) * (W/nf + 0.29)' ps='2*int((nf+2)/2) * (W/nf + 0.29)' nrd='0.29 / W' nrs='0.29 / W'
+ sa=0 sb=0 sd=0 mult=1 m=1
XM74 GND net2 VOUT GND sky130_fd_pr__nfet_01v8 L=.6 W=1.5 nf=1 ad='int((nf+1)/2) * W/nf * 0.29' as='int((nf+2)/2) * W/nf * 0.29'
+ pd='2*int((nf+1)/2) * (W/nf + 0.29)' ps='2*int((nf+2)/2) * (W/nf + 0.29)' nrd='0.29 / W' nrs='0.29 / W'
+ sa=0 sb=0 sd=0 mult=1 m=1
XM75 net21 net10 GND VDD sky130_fd_pr__pfet_01v8 L=.6 W=1.5 nf=1 ad='int((nf+1)/2) * W/nf * 0.29' as='int((nf+2)/2) * W/nf * 0.29'
+ pd='2*int((nf+1)/2) * (W/nf + 0.29)' ps='2*int((nf+2)/2) * (W/nf + 0.29)' nrd='0.29 / W' nrs='0.29 / W'
+ sa=0 sb=0 sd=0 mult=1 m=1
XM76 net10 net10 net4 VDD sky130_fd_pr__pfet_01v8 L=.6 W=1.5 nf=1 ad='int((nf+1)/2) * W/nf * 0.29' as='int((nf+2)/2) * W/nf * 0.29'
+ pd='2*int((nf+1)/2) * (W/nf + 0.29)' ps='2*int((nf+2)/2) * (W/nf + 0.29)' nrd='0.29 / W' nrs='0.29 / W'
+ sa=0 sb=0 sd=0 mult=1 m=1
XM77 net17 net9 VDD GND sky130_fd_pr__nfet_01v8 L=.6 W=1.5 nf=1 ad='int((nf+1)/2) * W/nf * 0.29' as='int((nf+2)/2) * W/nf * 0.29'
+ pd='2*int((nf+1)/2) * (W/nf + 0.29)' ps='2*int((nf+2)/2) * (W/nf + 0.29)' nrd='0.29 / W' nrs='0.29 / W'
+ sa=0 sb=0 sd=0 mult=1 m=1
XM78 net9 net9 net7 GND sky130_fd_pr__nfet_01v8 L=.6 W=1.5 nf=1 ad='int((nf+1)/2) * W/nf * 0.29' as='int((nf+2)/2) * W/nf * 0.29'
+ pd='2*int((nf+1)/2) * (W/nf + 0.29)' ps='2*int((nf+2)/2) * (W/nf + 0.29)' nrd='0.29 / W' nrs='0.29 / W'
+ sa=0 sb=0 sd=0 mult=1 m=1
XMD79 VDD GND GND GND sky130_fd_pr__nfet_01v8 L=.6 W=1.5 nf=1 ad='int((nf+1)/2) * W/nf * 0.29' as='int((nf+2)/2) * W/nf * 0.29'
+ pd='2*int((nf+1)/2) * (W/nf + 0.29)' ps='2*int((nf+2)/2) * (W/nf + 0.29)' nrd='0.29 / W' nrs='0.29 / W'
+ sa=0 sb=0 sd=0 mult=1 m=1
XMD80 net7 GND GND GND sky130_fd_pr__nfet_01v8 L=.6 W=1.5 nf=1 ad='int((nf+1)/2) * W/nf * 0.29' as='int((nf+2)/2) * W/nf * 0.29'
+ pd='2*int((nf+1)/2) * (W/nf + 0.29)' ps='2*int((nf+2)/2) * (W/nf + 0.29)' nrd='0.29 / W' nrs='0.29 / W'
+ sa=0 sb=0 sd=0 mult=1 m=1
XMD81 GND VDD VDD VDD sky130_fd_pr__pfet_01v8 L=.6 W=1.5 nf=1 ad='int((nf+1)/2) * W/nf * 0.29' as='int((nf+2)/2) * W/nf * 0.29'
+ pd='2*int((nf+1)/2) * (W/nf + 0.29)' ps='2*int((nf+2)/2) * (W/nf + 0.29)' nrd='0.29 / W' nrs='0.29 / W'
+ sa=0 sb=0 sd=0 mult=1 m=1
XMD82 net4 VDD VDD VDD sky130_fd_pr__pfet_01v8 L=.6 W=1.5 nf=1 ad='int((nf+1)/2) * W/nf * 0.29' as='int((nf+2)/2) * W/nf * 0.29'
+ pd='2*int((nf+1)/2) * (W/nf + 0.29)' ps='2*int((nf+2)/2) * (W/nf + 0.29)' nrd='0.29 / W' nrs='0.29 / W'
+ sa=0 sb=0 sd=0 mult=1 m=1
XMD83 net24 GND net3 GND sky130_fd_pr__nfet_01v8 L=.6 W=1.5 nf=1 ad='int((nf+1)/2) * W/nf * 0.29' as='int((nf+2)/2) * W/nf * 0.29'
+ pd='2*int((nf+1)/2) * (W/nf + 0.29)' ps='2*int((nf+2)/2) * (W/nf + 0.29)' nrd='0.29 / W' nrs='0.29 / W'
+ sa=0 sb=0 sd=0 mult=1 m=1
XMD84 net25 GND net4 GND sky130_fd_pr__nfet_01v8 L=.6 W=1.5 nf=1 ad='int((nf+1)/2) * W/nf * 0.29' as='int((nf+2)/2) * W/nf * 0.29'
+ pd='2*int((nf+1)/2) * (W/nf + 0.29)' ps='2*int((nf+2)/2) * (W/nf + 0.29)' nrd='0.29 / W' nrs='0.29 / W'
+ sa=0 sb=0 sd=0 mult=1 m=1
XMD85 net22 VDD net6 VDD sky130_fd_pr__pfet_01v8 L=.6 W=1.5 nf=1 ad='int((nf+1)/2) * W/nf * 0.29' as='int((nf+2)/2) * W/nf * 0.29'
+ pd='2*int((nf+1)/2) * (W/nf + 0.29)' ps='2*int((nf+2)/2) * (W/nf + 0.29)' nrd='0.29 / W' nrs='0.29 / W'
+ sa=0 sb=0 sd=0 mult=1 m=1
XMD86 net23 VDD net7 VDD sky130_fd_pr__pfet_01v8 L=.6 W=1.5 nf=1 ad='int((nf+1)/2) * W/nf * 0.29' as='int((nf+2)/2) * W/nf * 0.29'
+ pd='2*int((nf+1)/2) * (W/nf + 0.29)' ps='2*int((nf+2)/2) * (W/nf + 0.29)' nrd='0.29 / W' nrs='0.29 / W'
+ sa=0 sb=0 sd=0 mult=1 m=1
XC1 net2 VOUT sky130_fd_pr__cap_mim_m3_1 W=20 L=12 MF=1 m=1
.ends

.GLOBAL GND
.GLOBAL VDD
.end
